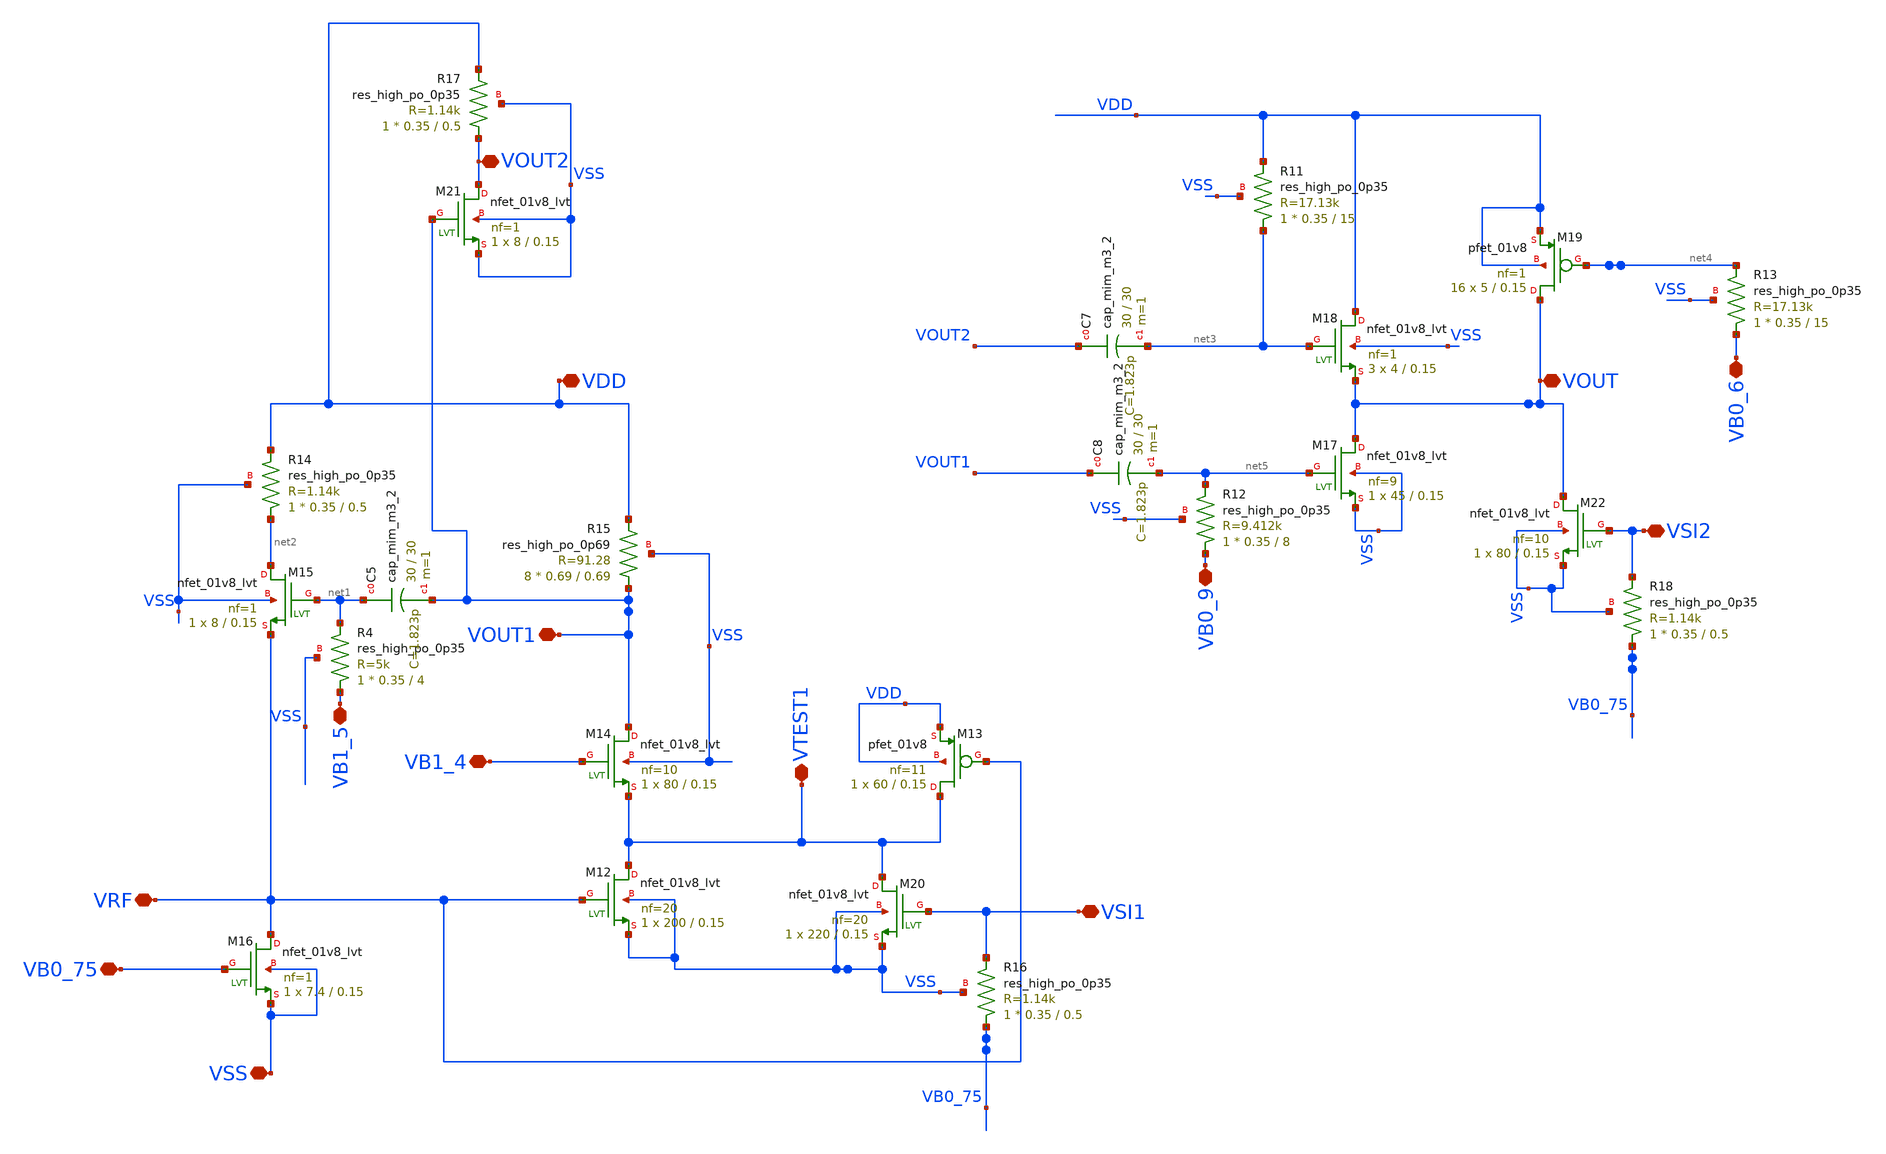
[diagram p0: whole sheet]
** sch_path: xschem/xschem4_sic_final/2stage_for_symbol.sch
**.subckt 2stage_for_symbol VRF VSS VB0_75 VSI1 VDD VOUT1 VOUT2 VB1_4 VB1_5 VB0_9 VSI2 VB0_6 VTEST1
*+ VOUT
*.iopin VRF
*.iopin VSS
*.iopin VB0_75
*.iopin VSI1
*.iopin VDD
*.iopin VOUT1
*.iopin VOUT2
*.iopin VB1_4
*.iopin VB1_5
*.iopin VB0_9
*.iopin VSI2
*.iopin VB0_6
*.iopin VTEST1
*.iopin VOUT
XR4 VB1_5 net1 VSS sky130_fd_pr__res_high_po_0p35 L=4 mult=1 m=1
XC5 net1 VOUT1 sky130_fd_pr__cap_mim_m3_2 W=30 L=30 MF=1 m=1
XM12 VTEST1 VRF VSS VSS sky130_fd_pr__nfet_01v8_lvt L=0.15 W=200 nf=20 ad='int((nf+1)/2) * W/nf * 0.29'
+ as='int((nf+2)/2) * W/nf * 0.29' pd='2*int((nf+1)/2) * (W/nf + 0.29)' ps='2*int((nf+2)/2) * (W/nf + 0.29)'
+ nrd='0.29 / W' nrs='0.29 / W' sa=0 sb=0 sd=0 mult=1 m=1
XM13 VTEST1 VRF VDD VDD sky130_fd_pr__pfet_01v8 L=0.15 W=60 nf=11 ad='int((nf+1)/2) * W/nf * 0.29' as='int((nf+2)/2) * W/nf * 0.29'
+ pd='2*int((nf+1)/2) * (W/nf + 0.29)' ps='2*int((nf+2)/2) * (W/nf + 0.29)' nrd='0.29 / W' nrs='0.29 / W'
+ sa=0 sb=0 sd=0 mult=1 m=1
XM14 VOUT1 VB1_4 VTEST1 VSS sky130_fd_pr__nfet_01v8_lvt L=0.15 W=80 nf=10 ad='int((nf+1)/2) * W/nf * 0.29'
+ as='int((nf+2)/2) * W/nf * 0.29' pd='2*int((nf+1)/2) * (W/nf + 0.29)' ps='2*int((nf+2)/2) * (W/nf + 0.29)'
+ nrd='0.29 / W' nrs='0.29 / W' sa=0 sb=0 sd=0 mult=1 m=1
XM15 net2 net1 VRF VSS sky130_fd_pr__nfet_01v8_lvt L=0.15 W=8 nf=1 ad='int((nf+1)/2) * W/nf * 0.29' as='int((nf+2)/2) * W/nf * 0.29'
+ pd='2*int((nf+1)/2) * (W/nf + 0.29)' ps='2*int((nf+2)/2) * (W/nf + 0.29)' nrd='0.29 / W' nrs='0.29 / W'
+ sa=0 sb=0 sd=0 mult=1 m=1
XM16 VRF VB0_75 VSS VSS sky130_fd_pr__nfet_01v8_lvt L=0.15 W=7.4 nf=1 ad='int((nf+1)/2) * W/nf * 0.29'
+ as='int((nf+2)/2) * W/nf * 0.29' pd='2*int((nf+1)/2) * (W/nf + 0.29)' ps='2*int((nf+2)/2) * (W/nf + 0.29)'
+ nrd='0.29 / W' nrs='0.29 / W' sa=0 sb=0 sd=0 mult=1 m=1
XM17 VOUT net5 VSS VSS sky130_fd_pr__nfet_01v8_lvt L=0.15 W=45 nf=9 ad='int((nf+1)/2) * W/nf * 0.29'
+ as='int((nf+2)/2) * W/nf * 0.29' pd='2*int((nf+1)/2) * (W/nf + 0.29)' ps='2*int((nf+2)/2) * (W/nf + 0.29)'
+ nrd='0.29 / W' nrs='0.29 / W' sa=0 sb=0 sd=0 mult=1 m=1
XM18 VDD net3 VOUT VSS sky130_fd_pr__nfet_01v8_lvt L=0.15 W=4 nf=1 ad='int((nf+1)/2) * W/nf * 0.29' as='int((nf+2)/2) * W/nf * 0.29'
+ pd='2*int((nf+1)/2) * (W/nf + 0.29)' ps='2*int((nf+2)/2) * (W/nf + 0.29)' nrd='0.29 / W' nrs='0.29 / W'
+ sa=0 sb=0 sd=0 mult=3 m=3
XR11 net3 VDD VSS sky130_fd_pr__res_high_po_0p35 L=15 mult=1 m=1
XM19 VOUT net4 VDD VDD sky130_fd_pr__pfet_01v8 L=0.15 W=5 nf=1 ad='int((nf+1)/2) * W/nf * 0.29' as='int((nf+2)/2) * W/nf * 0.29'
+ pd='2*int((nf+1)/2) * (W/nf + 0.29)' ps='2*int((nf+2)/2) * (W/nf + 0.29)' nrd='0.29 / W' nrs='0.29 / W'
+ sa=0 sb=0 sd=0 mult=16 m=16
XC7 VOUT2 net3 sky130_fd_pr__cap_mim_m3_2 W=30 L=30 MF=1 m=1
XR12 VB0_9 net5 VSS sky130_fd_pr__res_high_po_0p35 L=8 mult=1 m=1
XC8 VOUT1 net5 sky130_fd_pr__cap_mim_m3_2 W=30 L=30 MF=1 m=1
XR13 VB0_6 net4 VSS sky130_fd_pr__res_high_po_0p35 L=15 mult=1 m=1
XR14 net2 VDD VSS sky130_fd_pr__res_high_po_0p35 L=0.5 mult=1 m=1
XM20 VTEST1 VSI1 VSS VSS sky130_fd_pr__nfet_01v8_lvt L=0.15 W=220 nf=20 ad='int((nf+1)/2) * W/nf * 0.29'
+ as='int((nf+2)/2) * W/nf * 0.29' pd='2*int((nf+1)/2) * (W/nf + 0.29)' ps='2*int((nf+2)/2) * (W/nf + 0.29)'
+ nrd='0.29 / W' nrs='0.29 / W' sa=0 sb=0 sd=0 mult=1 m=1
XR15 VOUT1 VDD VSS sky130_fd_pr__res_high_po_0p69 L=0.69 mult=8 m=8
XR16 VB0_75 VSI1 VSS sky130_fd_pr__res_high_po_0p35 L=0.5 mult=1 m=1
XM21 VOUT2 VOUT1 VSS VSS sky130_fd_pr__nfet_01v8_lvt L=0.15 W=8 nf=1 ad='int((nf+1)/2) * W/nf * 0.29'
+ as='int((nf+2)/2) * W/nf * 0.29' pd='2*int((nf+1)/2) * (W/nf + 0.29)' ps='2*int((nf+2)/2) * (W/nf + 0.29)'
+ nrd='0.29 / W' nrs='0.29 / W' sa=0 sb=0 sd=0 mult=1 m=1
XR17 VOUT2 VDD VSS sky130_fd_pr__res_high_po_0p35 L=0.5 mult=1 m=1
XM22 VOUT VSI2 VSS VSS sky130_fd_pr__nfet_01v8_lvt L=0.15 W=80 nf=10 ad='int((nf+1)/2) * W/nf * 0.29'
+ as='int((nf+2)/2) * W/nf * 0.29' pd='2*int((nf+1)/2) * (W/nf + 0.29)' ps='2*int((nf+2)/2) * (W/nf + 0.29)'
+ nrd='0.29 / W' nrs='0.29 / W' sa=0 sb=0 sd=0 mult=1 m=1
XR18 VB0_75 VSI2 VSS sky130_fd_pr__res_high_po_0p35 L=0.5 mult=1 m=1
**** begin user architecture code

.lib $::SKYWATER_MODELS/sky130.lib.spice tt

**** end user architecture code
**.ends
.end
